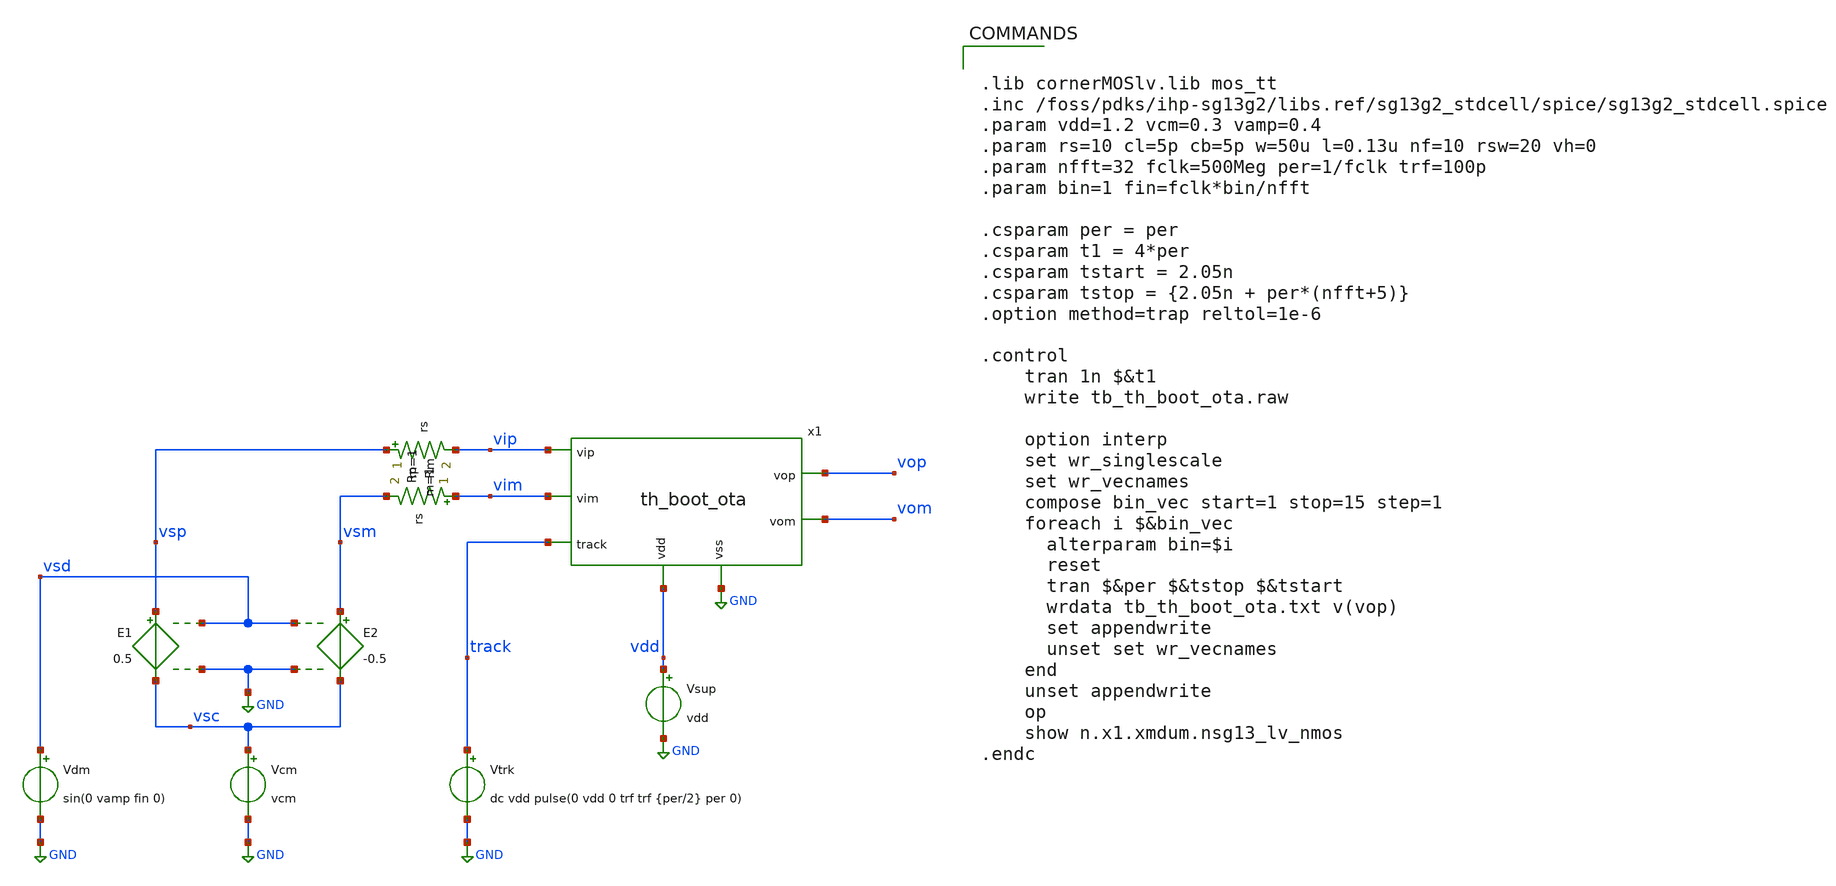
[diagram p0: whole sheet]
** sch_path: old/xschem/tb_th_boot_ota.sch
**.subckt tb_th_boot_ota
E1 vsp vsc vsd GND 0.5
E2 vsm vsc vsd GND -0.5
Vcm vsc GND vcm
Vsup vdd GND vdd
Vdm vsd GND sin(0 vamp fin 0)
x1 track vip vop vom vim GND vdd th_boot_ota
Rp vsp vip rs m=1
Rm vim vsm rs m=1
Vtrk track GND dc vdd pulse(0 vdd 0 trf trf {per/2} per 0)
**** begin user architecture code


.lib cornerMOSlv.lib mos_tt
.inc /foss/pdks/ihp-sg13g2/libs.ref/sg13g2_stdcell/spice/sg13g2_stdcell.spice
.param vdd=1.2 vcm=0.3 vamp=0.4
.param rs=10 cl=5p cb=5p w=50u l=0.13u nf=10 rsw=20 vh=0
.param nfft=32 fclk=500Meg per=1/fclk trf=100p
.param bin=1 fin=fclk*bin/nfft

.csparam per = per
.csparam t1 = 4*per
.csparam tstart = 2.05n
.csparam tstop = {2.05n + per*(nfft+5)}
.option method=trap reltol=1e-6

.control
    tran 1n $&t1
    write tb_th_boot_ota.raw

    option interp
    set wr_singlescale
    set wr_vecnames
    compose bin_vec start=1 stop=15 step=1
    foreach i $&bin_vec
      alterparam bin=$i
      reset
      tran $&per $&tstop $&tstart
      wrdata tb_th_boot_ota.txt v(vop)
      set appendwrite
      unset set wr_vecnames
    end
    unset appendwrite
    op
    show n.x1.xmdum.nsg13_lv_nmos
.endc


**** end user architecture code
**.ends
.GLOBAL GND
.end
